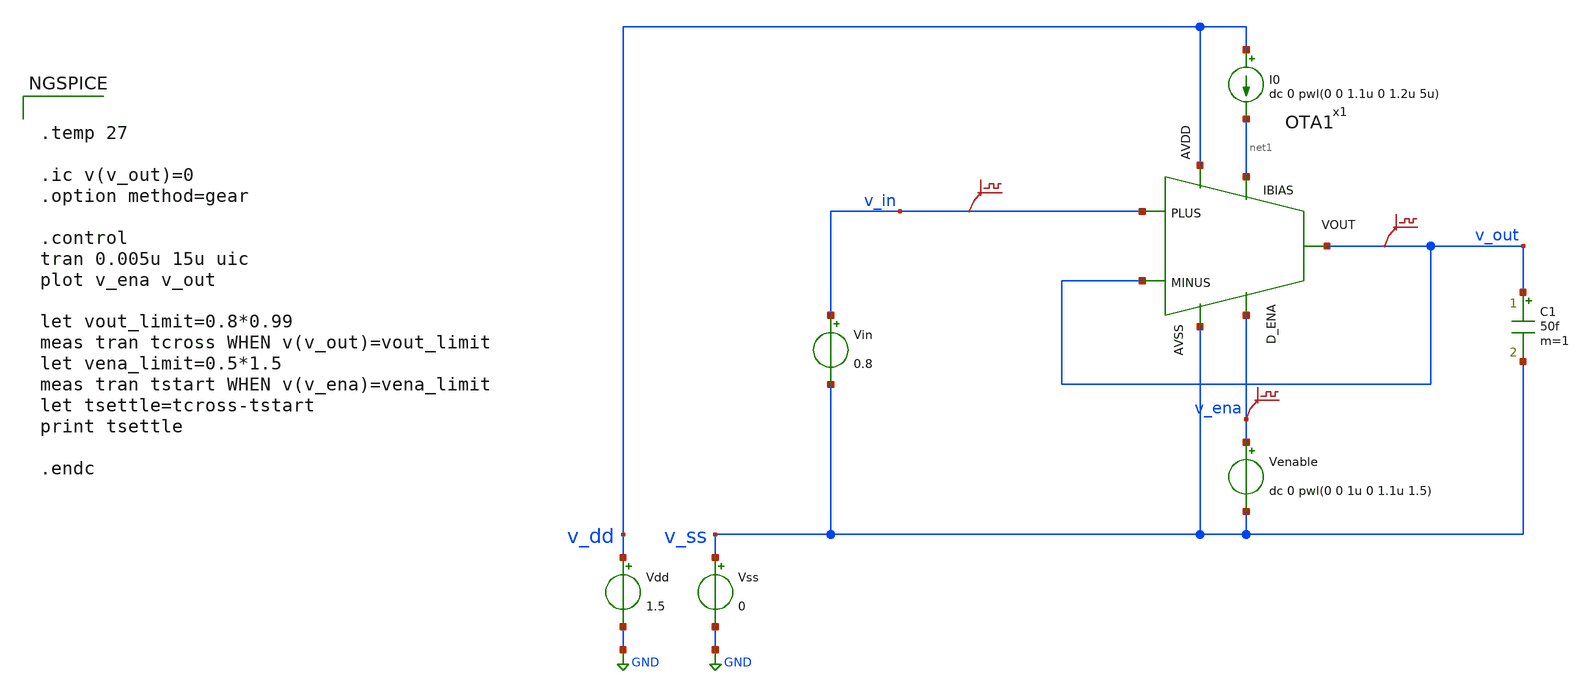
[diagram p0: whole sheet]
** sch_path: DSM_2ndOrder/1_Schematics/real_circuits/3v3/tb_ota1_tran.sch
* DSM_2ndOrder/1_Schematics/real_circuits/3v3/OTA1.sch:
* (c) 2025 Thesis_HP, Apache-2.0 license
**.subckt tb_ota1_tran
Vdd v_dd GND 1.5
Vss v_ss GND 0
C1 v_out v_ss 50f m=1
Vin v_in v_ss 0.8
I0 v_dd net1 dc 0 pwl(0 0 1.1u 0 1.2u 5u)
Venable v_ena v_ss dc 0 pwl(0 0 1u 0 1.1u 1.5)
.save v(v_in)
.save v(v_out)
.save v(v_ena)
x1 v_dd net1 v_out v_out v_in v_ena v_ss OTA1
**** begin user architecture code


.temp 27

.ic v(v_out)=0
.option method=gear

.control
tran 0.005u 15u uic
plot v_ena v_out

let vout_limit=0.8*0.99
meas tran tcross WHEN v(v_out)=vout_limit
let vena_limit=0.5*1.5
meas tran tstart WHEN v(v_ena)=vena_limit
let tsettle=tcross-tstart
print tsettle

.endc


**** end user architecture code
**.ends

* expanding   symbol:  OTA1.sym # of pins=7
** sym_path: DSM_2ndOrder/1_Schematics/real_circuits/3v3/OTA1.sym
** sch_path: DSM_2ndOrder/1_Schematics/real_circuits/3v3/OTA1.sch
.subckt OTA1 AVDD IBIAS VOUT MINUS PLUS D_ENA AVSS
*.ipin AVSS
*.ipin IBIAS
*.ipin AVDD
*.ipin PLUS
*.ipin MINUS
*.opin VOUT
*.ipin D_ENA
XM23 IBIAS net3 AVSS AVSS sg13_hv_nmos w=13.8u l=1u ng=2 m=1 mm_ok=1
XM25 IBIAS net2 net3 AVSS sg13_hv_nmos w=1u l=0.5u ng=1 m=1 mm_ok=1
XM24 net10 net3 AVSS AVSS sg13_hv_nmos w=13.8u l=1u ng=2 m=1 mm_ok=1
XM19 net10 net5 net4 AVDD sg13_hv_pmos w=42.5u l=1u ng=10 m=1 mm_ok=1
XM20 net4 net4 AVDD AVDD sg13_hv_pmos w=42.5u l=1u ng=10 m=1 mm_ok=1
XM21 AVSS net5 net8 AVDD sg13_hv_pmos w=100u l=0.5u ng=10 m=1 mm_ok=1
XM22 net8 net4 AVDD AVDD sg13_hv_pmos w=42.5u l=1u ng=10 m=1 mm_ok=1
XM26 net7 net4 AVDD AVDD sg13_hv_pmos w=85.5u l=1u ng=10 m=1 mm_ok=1
XM27 net5 net8 net7 AVDD sg13_hv_pmos w=42.5u l=1u ng=10 m=1 mm_ok=1
XM28 net5 net15 net6 AVSS sg13_hv_nmos w=12u l=1u ng=2 m=1 mm_ok=1
XM29 net6 net5 AVSS AVSS sg13_hv_nmos w=12.5u l=1u ng=2 m=1 mm_ok=1
XM30 net9 net3 AVSS AVSS sg13_hv_nmos w=14u l=1u ng=2 m=1 mm_ok=1
XM31 net7 PLUS net9 AVSS sg13_hv_nmos w=14.5u l=0.8u ng=2 m=1 mm_ok=1
XM32 net11 MINUS net9 AVSS sg13_hv_nmos w=14.5u l=0.8u ng=2 m=1 mm_ok=1
XM42 AVDD net4 AVDD AVDD sg13_hv_pmos w=12u l=0.5u ng=4 m=1 mm_ok=1
XM41 AVDD net8 AVDD AVDD sg13_hv_pmos w=12u l=0.5u ng=4 m=1 mm_ok=1
XM38 AVSS net3 AVSS AVSS sg13_hv_nmos w=8u l=1u ng=4 m=1 mm_ok=1
XM33 net1 D_ENA AVDD AVDD sg13_hv_pmos w=1u l=0.5u ng=1 m=1 mm_ok=1
XM34 net2 net1 AVDD AVDD sg13_hv_pmos w=1u l=0.5u ng=1 m=1 mm_ok=1
XM35 net1 D_ENA AVSS AVSS sg13_hv_nmos w=1u l=0.5u ng=1 m=1 mm_ok=1
XM36 net2 net1 AVSS AVSS sg13_hv_nmos w=1u l=0.5u ng=1 m=1 mm_ok=1
XM37 net11 AVSS AVSS AVSS sg13_hv_nmos w=14.5u l=0.8u ng=2 m=1 mm_ok=1
XM39 VOUT net8 net11 AVDD sg13_hv_pmos w=42.5u l=1u ng=10 m=1 mm_ok=1
XM40 net11 net4 AVDD AVDD sg13_hv_pmos w=85.5u l=1u ng=10 m=1 mm_ok=1
XM43 VOUT net15 net12 AVSS sg13_hv_nmos w=12u l=1u ng=2 m=1 mm_ok=1
XM44 net12 net5 AVSS AVSS sg13_hv_nmos w=12.5u l=1u ng=2 m=1 mm_ok=1
XM45 net12 AVSS AVSS AVSS sg13_hv_nmos w=12.5u l=1u ng=2 m=1 mm_ok=1
XM46 VOUT AVSS AVSS AVSS sg13_hv_nmos w=12u l=1u ng=2 m=1 mm_ok=1
XM47 net11 AVDD AVDD AVDD sg13_hv_pmos w=85.5u l=1u ng=10 m=1 mm_ok=1
XM48 VOUT AVDD AVDD AVDD sg13_hv_pmos w=42.5u l=1u ng=10 m=1 mm_ok=1
XM49 net13 net4 AVDD AVDD sg13_hv_pmos w=85.5u l=1u ng=10 m=1 mm_ok=1
XM50 net13 VOUT net14 AVSS sg13_hv_nmos w=12u l=1u ng=2 m=1 mm_ok=1
XM51 net14 net14 AVSS AVSS sg13_hv_nmos w=12u l=1u ng=2 m=1 mm_ok=1
XM52 net15 net14 AVSS AVSS sg13_hv_nmos w=12u l=1u ng=2 m=1 mm_ok=1
XM53 AVDD VOUT net15 AVSS sg13_hv_nmos w=100u l=0.5u ng=10 m=1 mm_ok=1
XM54 AVSS net15 AVSS AVSS sg13_hv_nmos w=8u l=1u ng=4 m=1 mm_ok=1
XM55 net5 net1 AVSS AVSS sg13_hv_nmos w=1u l=0.5u ng=1 m=1 mm_ok=1
XM56 net7 AVSS AVSS AVSS sg13_hv_nmos w=14.5u l=0.8u ng=2 m=1 mm_ok=1
XM57 net5 AVDD AVDD AVDD sg13_hv_pmos w=42.5u l=1u ng=10 m=1 mm_ok=1
XM58 net6 AVSS AVSS AVSS sg13_hv_nmos w=12.5u l=1u ng=2 m=1 mm_ok=1
XM59 net5 AVSS AVSS AVSS sg13_hv_nmos w=12u l=1u ng=2 m=1 mm_ok=1
XM60 net4 AVDD AVDD AVDD sg13_hv_pmos w=42.5u l=1u ng=10 m=1 mm_ok=1
XM61 net14 AVSS AVSS AVSS sg13_hv_nmos w=12u l=1u ng=2 m=1 mm_ok=1
.ends

.GLOBAL GND
.end
